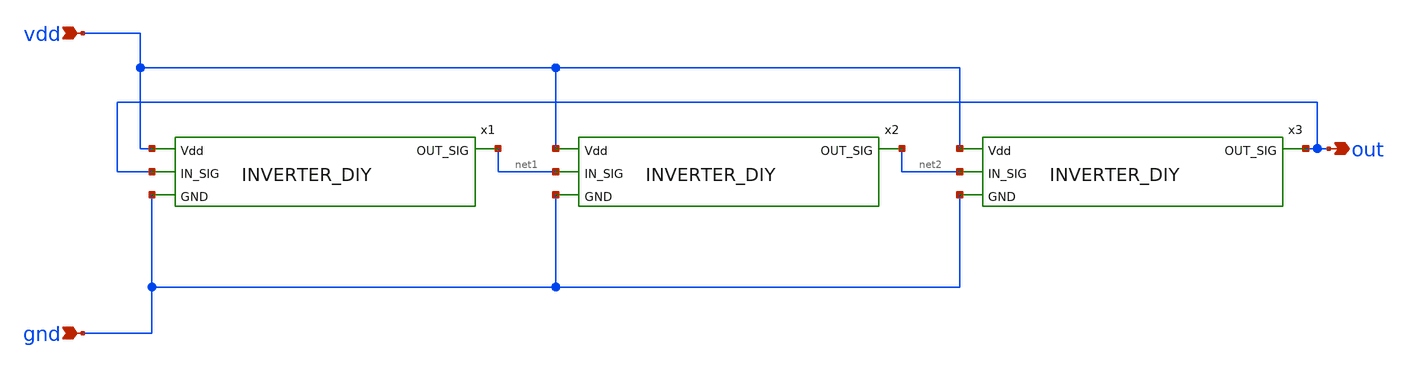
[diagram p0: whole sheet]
** sch_path: ringoscillator_backup/ringoscillator3bak.sch
**.subckt ringoscillator3bak vdd gnd out
*.ipin vdd
*.ipin gnd
*.opin out
x1 vdd out net1 gnd INVERTER_DIY
x2 vdd net1 net2 gnd INVERTER_DIY
x3 vdd net2 out gnd INVERTER_DIY
**.ends
.end
